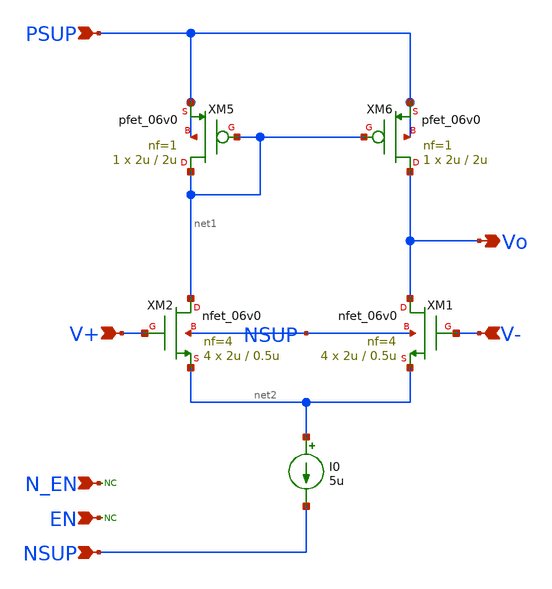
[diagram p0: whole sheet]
** sch_path: xschem/lib/aux_amp.sch
**.subckt aux_amp PSUP NSUP N_EN EN V+ V- Vo
*.ipin PSUP
*.ipin NSUP
*.ipin N_EN
*.ipin EN
*.ipin V+
*.ipin V-
*.opin Vo
XM1 Vo V- net2 NSUP nfet_06v0 L=0.5u W=2u nf=4 ad='int((nf+1)/2) * W/nf * 0.18u' as='int((nf+2)/2) * W/nf * 0.18u'
+ pd='2*int((nf+1)/2) * (W/nf + 0.18u)' ps='2*int((nf+2)/2) * (W/nf + 0.18u)' nrd='0.18u / W' nrs='0.18u / W'
+ sa=0 sb=0 sd=0 m=4
XM2 net1 V+ net2 NSUP nfet_06v0 L=0.5u W=2u nf=4 ad='int((nf+1)/2) * W/nf * 0.18u' as='int((nf+2)/2) * W/nf * 0.18u'
+ pd='2*int((nf+1)/2) * (W/nf + 0.18u)' ps='2*int((nf+2)/2) * (W/nf + 0.18u)' nrd='0.18u / W' nrs='0.18u / W'
+ sa=0 sb=0 sd=0 m=4
XM5 net1 net1 PSUP PSUP pfet_06v0 L=2u W=2u nf=1 ad='int((nf+1)/2) * W/nf * 0.18u' as='int((nf+2)/2) * W/nf * 0.18u'
+ pd='2*int((nf+1)/2) * (W/nf + 0.18u)' ps='2*int((nf+2)/2) * (W/nf + 0.18u)' nrd='0.18u / W' nrs='0.18u / W'
+ sa=0 sb=0 sd=0 m=1
XM6 Vo net1 PSUP PSUP pfet_06v0 L=2u W=2u nf=1 ad='int((nf+1)/2) * W/nf * 0.18u' as='int((nf+2)/2) * W/nf * 0.18u'
+ pd='2*int((nf+1)/2) * (W/nf + 0.18u)' ps='2*int((nf+2)/2) * (W/nf + 0.18u)' nrd='0.18u / W' nrs='0.18u / W'
+ sa=0 sb=0 sd=0 m=1
I0 net2 NSUP 5u
* noconn N_EN
* noconn EN
**.ends
.end
